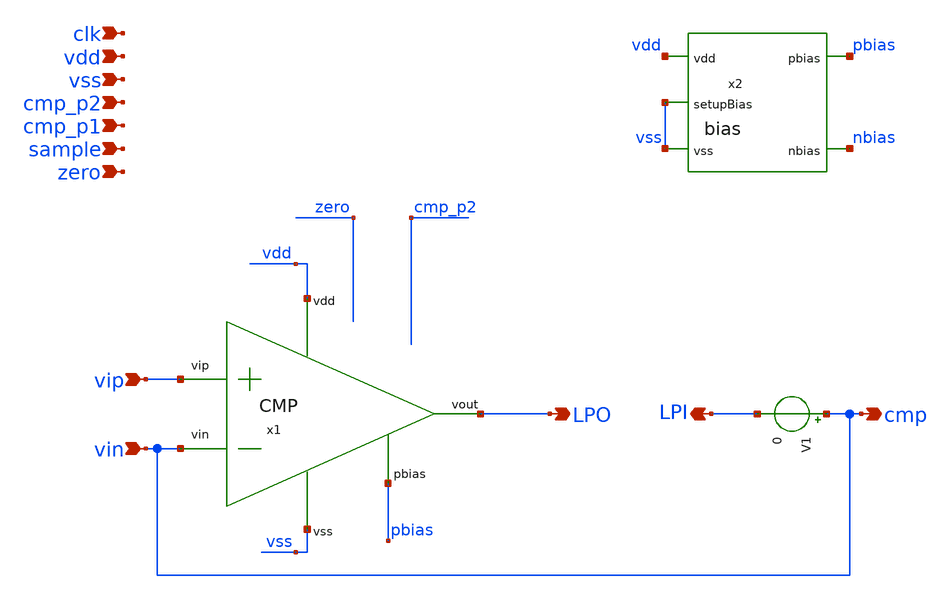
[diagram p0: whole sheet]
** sch_path: design/JNW_AVV_SKY130A/TB_CMP.sch
**.subckt TB_CMP vdd vss vip vin cmp cmp_p1 cmp_p2 clk sample zero LPI LPO
*.ipin vdd
*.ipin vss
*.ipin vip
*.ipin vin
*.opin cmp
*.ipin cmp_p1
*.ipin cmp_p2
*.ipin clk
*.ipin sample
*.ipin zero
*.opin LPI
*.opin LPO
x2 pbias vdd nbias vss vss bias
x1 vdd pbias LPO vin vip vss CMP
V1 vin LPI 0
**.ends
.end
